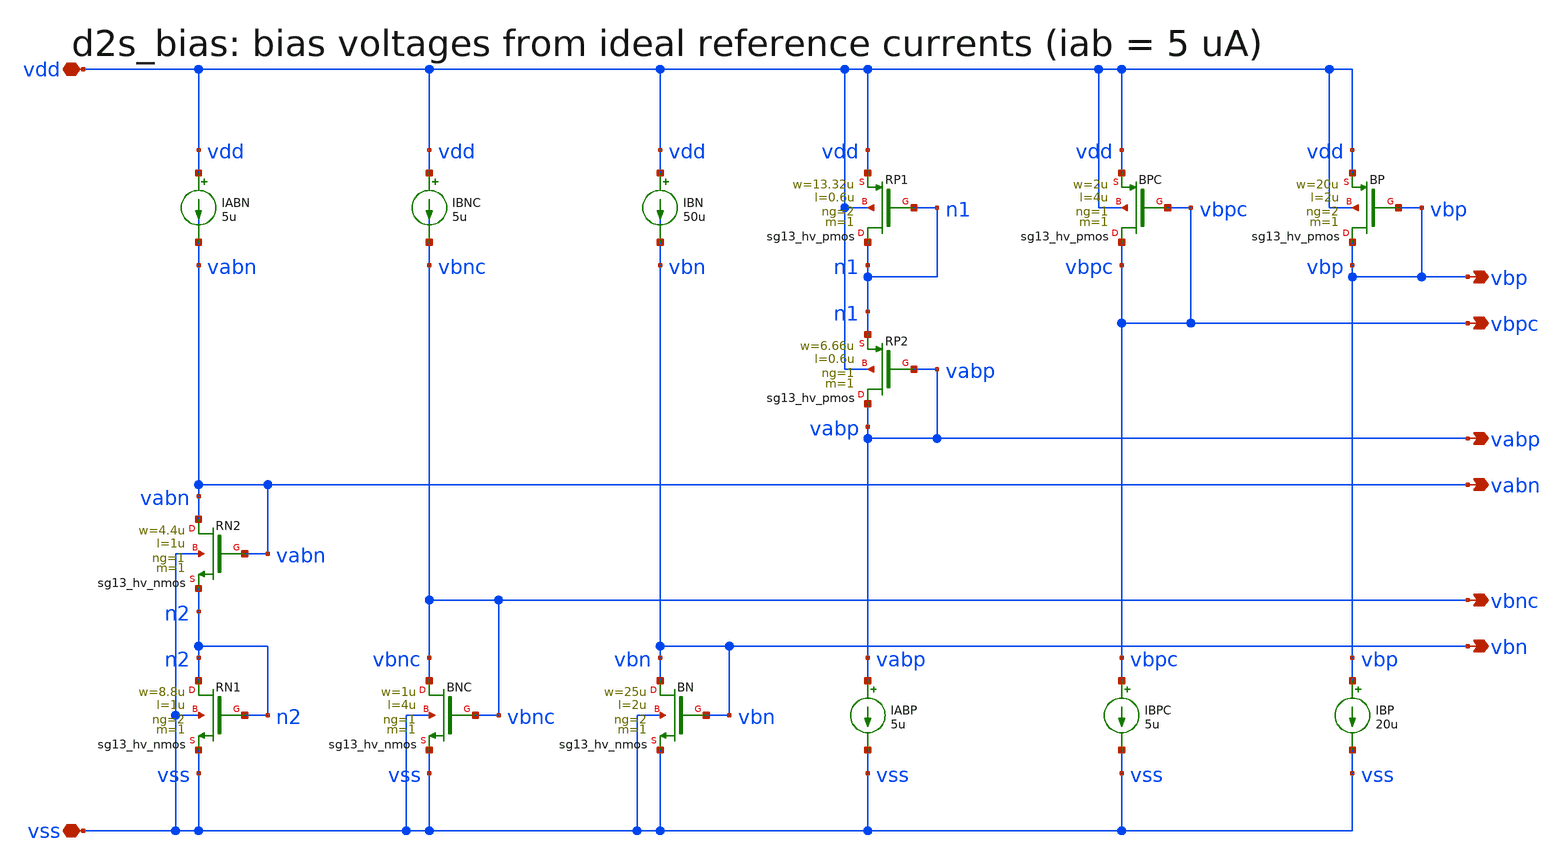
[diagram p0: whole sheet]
** sch_path: sudelbuecher/design_considerations/class_ab_pad_driver/xschem/d2s_bias.sch
**.subckt d2s_bias vdd vss vbp vbn vbpc vbnc vabp vabn
*.iopin vdd
*.iopin vss
*.opin vbp
*.opin vbn
*.opin vbpc
*.opin vbnc
*.opin vabp
*.opin vabn
IBP vbp vss 20u
XBP vbp vbp vdd vdd sg13_hv_pmos w=20u l=2u ng=2 m=1 mm_ok=1
IBN vdd vbn 50u
XBN vbn vbn vss vss sg13_hv_nmos w=25u l=2u ng=2 m=1 mm_ok=1
IBNC vdd vbnc 5u
XBNC vbnc vbnc vss vss sg13_hv_nmos w=1u l=4u ng=1 m=1 mm_ok=1
IBPC vbpc vss 5u
XBPC vbpc vbpc vdd vdd sg13_hv_pmos w=2u l=4u ng=1 m=1 mm_ok=1
IABP vabp vss 5u
XRP1 n1 n1 vdd vdd sg13_hv_pmos w=13.32u l=0.6u ng=2 m=1 mm_ok=1
XRP2 vabp vabp n1 vdd sg13_hv_pmos w=6.66u l=0.6u ng=1 m=1 mm_ok=1
IABN vdd vabn 5u
XRN1 n2 n2 vss vss sg13_hv_nmos w=8.8u l=1u ng=2 m=1 mm_ok=1
XRN2 vabn vabn n2 vss sg13_hv_nmos w=4.4u l=1u ng=1 m=1 mm_ok=1
**.ends
.end
